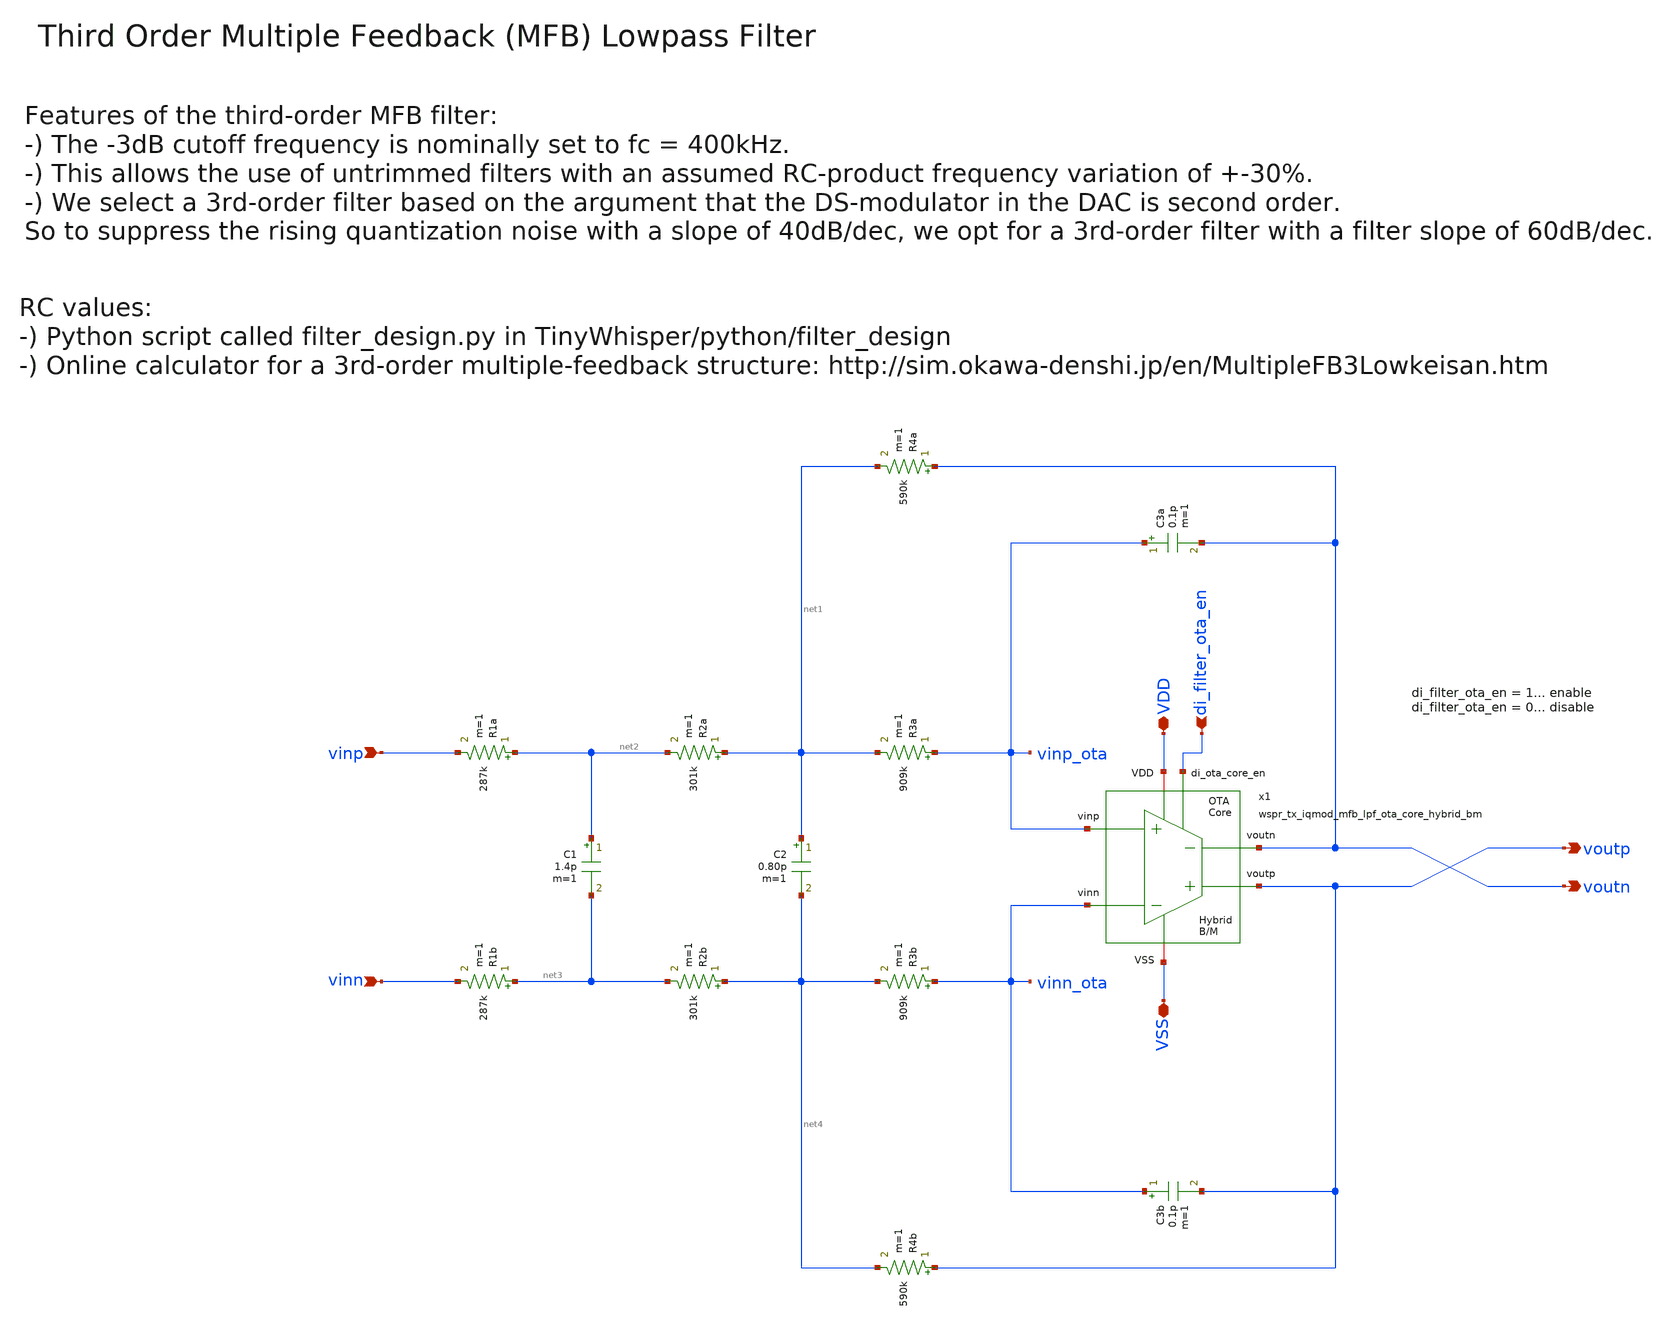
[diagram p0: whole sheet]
** sch_path: sky130/macros/iqmod/schematic/wspr_tx_iqmod_mfb_lpf_ideal.sch
**.subckt wspr_tx_iqmod_mfb_lpf_ideal VDD VSS di_filter_ota_en vinp vinn voutp voutn
*.iopin VDD
*.iopin VSS
*.ipin di_filter_ota_en
*.ipin vinp
*.ipin vinn
*.opin voutp
*.opin voutn
C1 net2 net3 1.4p m=1
C2 net1 net4 0.80p m=1
C3a vinp_ota voutn 0.1p m=1
C3b vinn_ota voutp 0.1p m=1
R1a net2 vinp 287k m=1
R1b net3 vinn 287k m=1
R2a net1 net2 301k m=1
R2b net4 net3 301k m=1
R3a vinp_ota net1 909k m=1
R3b vinn_ota net4 909k m=1
R4a voutn net1 590k m=1
R4b voutp net4 590k m=1
x1 di_filter_ota_en voutp voutn vinn_ota vinp_ota VDD VSS wspr_tx_iqmod_mfb_lpf_ota_core_hybrid_bm
**.ends
.end
